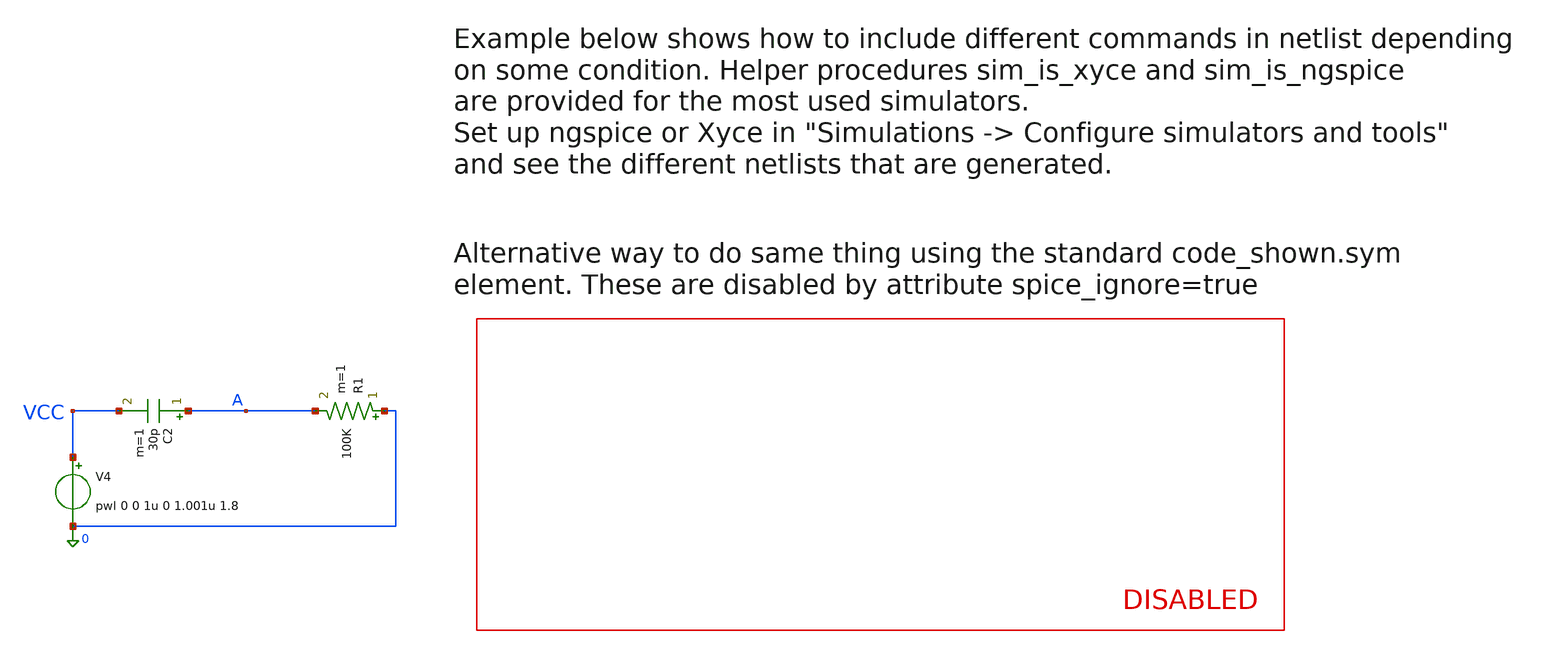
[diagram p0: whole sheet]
** sch_path: sky130A/xschem_libs/sky130_tests_ase/test_multisim/schematic/test_multisim.sch
* Copyright 2021 Stefan Frederik Schippers
* Licensed under the Apache License, Version 2.0 (the "License");
* you may not use this file except in compliance with the License.
* You may obtain a copy of the License at
* https://www.apache.org/licenses/LICENSE-2.0
* Unless required by applicable law or agreed to in writing, software
* distributed under the License is distributed on an "AS IS" BASIS,
* WITHOUT WARRANTIES OR CONDITIONS OF ANY KIND, either express or implied.
* See the License for the specific language governing permissions and
* limitations under the License.
**.subckt test_multisim
V4 VCC 0 pwl 0 0 1u 0 1.001u 1.8
R1 0 A 100K m=1
C2 A VCC 30p m=1
**.ends
.end
